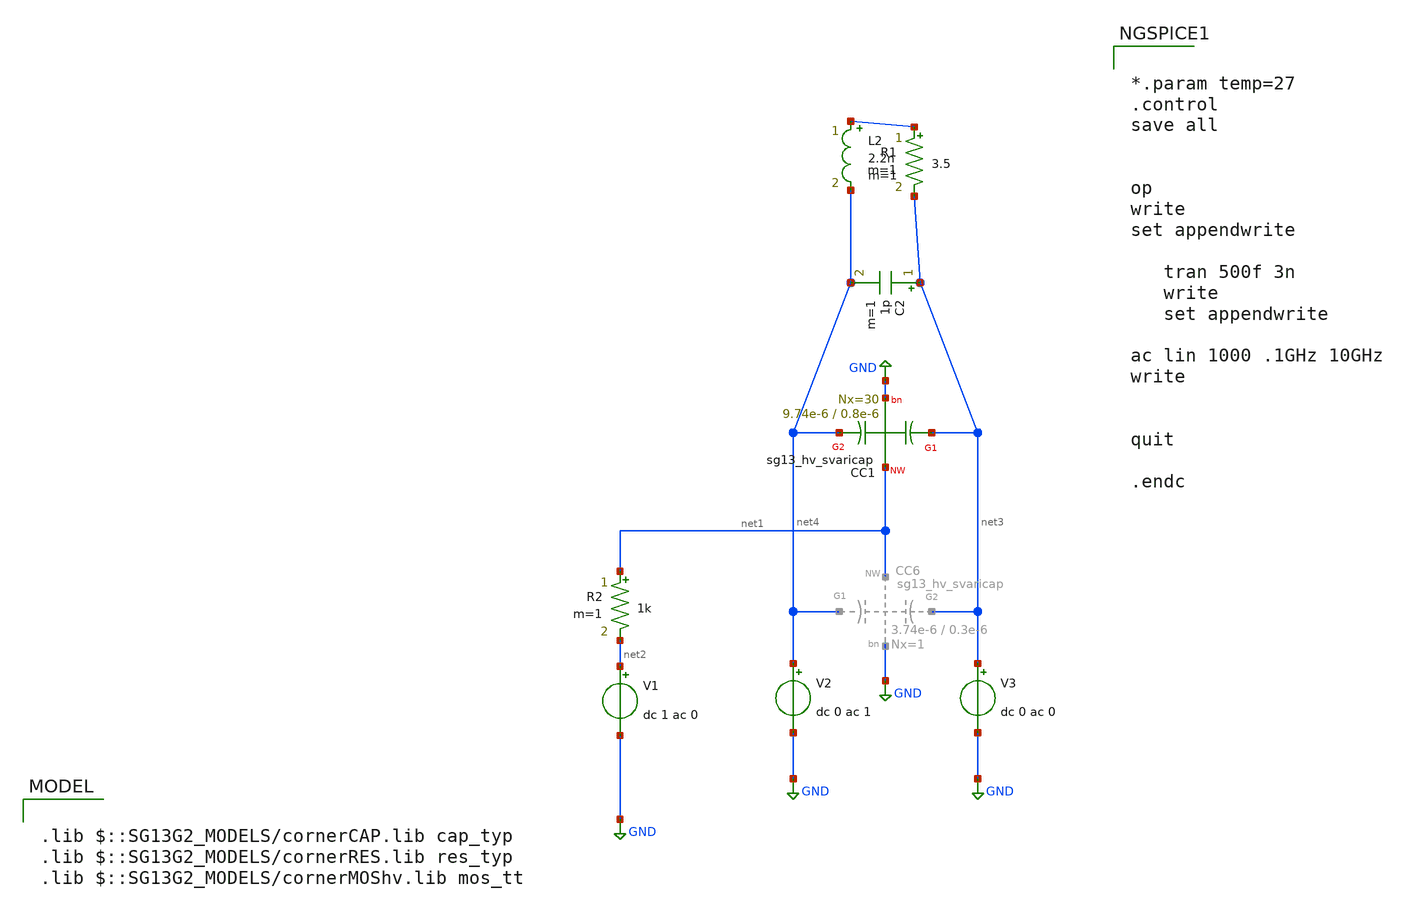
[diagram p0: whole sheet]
** sch_path: design_data/xschem/measuremenst_and_test_of_idas/ac_svaricap_test7tran.sch
**.subckt ac_svaricap_test7tran
V1 net2 GND dc 1 ac 0
V3 net3 GND dc 0 ac 0
V2 net4 GND dc 0 ac 1
XC1 net3 net1 net4 GND sg13_hv_svaricap w=9.74e-6 l=0.8e-6 Nx=30
C2 net3 net4 1p m=1
R1 net5 net3 3.5 m=1
L2 net5 net4 2.2n m=1
R2 net1 net2 1k m=1
**** begin user architecture code

.lib $::SG13G2_MODELS/cornerCAP.lib cap_typ
.lib $::SG13G2_MODELS/cornerRES.lib res_typ
.lib $::SG13G2_MODELS/cornerMOShv.lib mos_tt



*.param temp=27
.control
save all


op
write
set appendwrite

   tran 500f 3n
   write
   set appendwrite

ac lin 1000 .1GHz 10GHz
write


quit

.endc


**** end user architecture code
**.ends
.GLOBAL GND
.end
